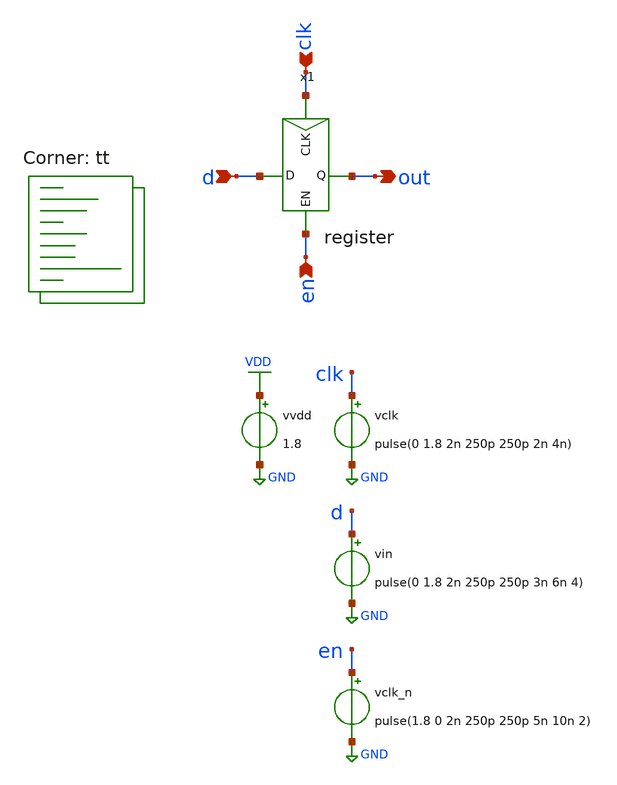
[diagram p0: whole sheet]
** sch_path: xschem/sim/tb_register.sch
**.subckt tb_register out en clk d
*.opin out
*.ipin en
*.ipin clk
*.ipin d
vvdd VDD GND 1.8
vclk clk GND pulse(0 1.8 2n 250p 250p 2n 4n)
vin d GND pulse(0 1.8 2n 250p 250p 3n 6n 4)
vclk_n en GND pulse(1.8 0 2n 250p 250p 5n 10n 2)
x1 clk en out d register
**** begin user architecture code
.lib $::SKYWATER_MODELS/sky130.lib.spice tt


.control
* Transient analysis
TRAN 1p 30n
save all
set filetype=binary
write tb_register_tran.raw
.endc


**** end user architecture code
**.ends

* expanding   symbol:  register.sym # of pins=4
** sym_path: xschem/register.sym
** sch_path: xschem/register.sch
.subckt register CLK EN Q D
*.ipin CLK
*.ipin EN
*.ipin D
*.opin Q
x1 net1 Q D d_flip_flop
x2 CLK EN net2 nand2
x3 net1 net2 inv
.ends


* expanding   symbol:  d_flip_flop.sym # of pins=3
** sym_path: xschem/d_flip_flop.sym
** sch_path: xschem/d_flip_flop.sch
.subckt d_flip_flop clk Q D
*.ipin clk
*.ipin D
*.opin Q
XM1 clk_b clk GND GND sky130_fd_pr__nfet_01v8 L=0.15 W=0.84 nf=1 ad='int((nf+1)/2) * W/nf * 0.29' as='int((nf+2)/2) * W/nf * 0.29'
+ pd='2*int((nf+1)/2) * (W/nf + 0.29)' ps='2*int((nf+2)/2) * (W/nf + 0.29)' nrd='0.29 / W' nrs='0.29 / W'
+ sa=0 sb=0 sd=0 mult=1 m=1
XM2 clk_b clk VDD VDD sky130_fd_pr__pfet_01v8 L=0.15 W=1.68 nf=1 ad='int((nf+1)/2) * W/nf * 0.29' as='int((nf+2)/2) * W/nf * 0.29'
+ pd='2*int((nf+1)/2) * (W/nf + 0.29)' ps='2*int((nf+2)/2) * (W/nf + 0.29)' nrd='0.29 / W' nrs='0.29 / W'
+ sa=0 sb=0 sd=0 mult=1 m=1
XM3 net1 clk net6 VDD sky130_fd_pr__pfet_01v8 L=0.15 W=0.42 nf=1 ad='int((nf+1)/2) * W/nf * 0.29' as='int((nf+2)/2) * W/nf * 0.29'
+ pd='2*int((nf+1)/2) * (W/nf + 0.29)' ps='2*int((nf+2)/2) * (W/nf + 0.29)' nrd='0.29 / W' nrs='0.29 / W'
+ sa=0 sb=0 sd=0 mult=1 m=1
XM4 net6 D VDD VDD sky130_fd_pr__pfet_01v8 L=0.15 W=0.42 nf=1 ad='int((nf+1)/2) * W/nf * 0.29' as='int((nf+2)/2) * W/nf * 0.29'
+ pd='2*int((nf+1)/2) * (W/nf + 0.29)' ps='2*int((nf+2)/2) * (W/nf + 0.29)' nrd='0.29 / W' nrs='0.29 / W'
+ sa=0 sb=0 sd=0 mult=1 m=1
XM5 net1 clk_b net5 GND sky130_fd_pr__nfet_01v8 L=0.15 W=0.42 nf=1 ad='int((nf+1)/2) * W/nf * 0.29' as='int((nf+2)/2) * W/nf * 0.29'
+ pd='2*int((nf+1)/2) * (W/nf + 0.29)' ps='2*int((nf+2)/2) * (W/nf + 0.29)' nrd='0.29 / W' nrs='0.29 / W'
+ sa=0 sb=0 sd=0 mult=1 m=1
XM6 net5 D GND GND sky130_fd_pr__nfet_01v8 L=0.15 W=0.42 nf=1 ad='int((nf+1)/2) * W/nf * 0.29' as='int((nf+2)/2) * W/nf * 0.29'
+ pd='2*int((nf+1)/2) * (W/nf + 0.29)' ps='2*int((nf+2)/2) * (W/nf + 0.29)' nrd='0.29 / W' nrs='0.29 / W'
+ sa=0 sb=0 sd=0 mult=1 m=1
XM7 net2 net1 VDD VDD sky130_fd_pr__pfet_01v8 L=0.15 W=0.42 nf=1 ad='int((nf+1)/2) * W/nf * 0.29' as='int((nf+2)/2) * W/nf * 0.29'
+ pd='2*int((nf+1)/2) * (W/nf + 0.29)' ps='2*int((nf+2)/2) * (W/nf + 0.29)' nrd='0.29 / W' nrs='0.29 / W'
+ sa=0 sb=0 sd=0 mult=1 m=1
XM8 net2 net1 GND GND sky130_fd_pr__nfet_01v8 L=0.15 W=0.42 nf=1 ad='int((nf+1)/2) * W/nf * 0.29' as='int((nf+2)/2) * W/nf * 0.29'
+ pd='2*int((nf+1)/2) * (W/nf + 0.29)' ps='2*int((nf+2)/2) * (W/nf + 0.29)' nrd='0.29 / W' nrs='0.29 / W'
+ sa=0 sb=0 sd=0 mult=1 m=1
XM9 net1 clk_b net4 VDD sky130_fd_pr__pfet_01v8 L=0.15 W=0.42 nf=1 ad='int((nf+1)/2) * W/nf * 0.29' as='int((nf+2)/2) * W/nf * 0.29'
+ pd='2*int((nf+1)/2) * (W/nf + 0.29)' ps='2*int((nf+2)/2) * (W/nf + 0.29)' nrd='0.29 / W' nrs='0.29 / W'
+ sa=0 sb=0 sd=0 mult=1 m=1
XM10 net4 net2 VDD VDD sky130_fd_pr__pfet_01v8 L=0.15 W=0.42 nf=1 ad='int((nf+1)/2) * W/nf * 0.29' as='int((nf+2)/2) * W/nf * 0.29'
+ pd='2*int((nf+1)/2) * (W/nf + 0.29)' ps='2*int((nf+2)/2) * (W/nf + 0.29)' nrd='0.29 / W' nrs='0.29 / W'
+ sa=0 sb=0 sd=0 mult=1 m=1
XM11 net1 clk net3 GND sky130_fd_pr__nfet_01v8 L=0.15 W=0.42 nf=1 ad='int((nf+1)/2) * W/nf * 0.29' as='int((nf+2)/2) * W/nf * 0.29'
+ pd='2*int((nf+1)/2) * (W/nf + 0.29)' ps='2*int((nf+2)/2) * (W/nf + 0.29)' nrd='0.29 / W' nrs='0.29 / W'
+ sa=0 sb=0 sd=0 mult=1 m=1
XM12 net3 net2 GND GND sky130_fd_pr__nfet_01v8 L=0.15 W=0.42 nf=1 ad='int((nf+1)/2) * W/nf * 0.29' as='int((nf+2)/2) * W/nf * 0.29'
+ pd='2*int((nf+1)/2) * (W/nf + 0.29)' ps='2*int((nf+2)/2) * (W/nf + 0.29)' nrd='0.29 / W' nrs='0.29 / W'
+ sa=0 sb=0 sd=0 mult=1 m=1
XM13 net7 clk_b net9 VDD sky130_fd_pr__pfet_01v8 L=0.15 W=0.42 nf=1 ad='int((nf+1)/2) * W/nf * 0.29'
+ as='int((nf+2)/2) * W/nf * 0.29' pd='2*int((nf+1)/2) * (W/nf + 0.29)' ps='2*int((nf+2)/2) * (W/nf + 0.29)'
+ nrd='0.29 / W' nrs='0.29 / W' sa=0 sb=0 sd=0 mult=1 m=1
XM14 net9 net2 VDD VDD sky130_fd_pr__pfet_01v8 L=0.15 W=0.42 nf=1 ad='int((nf+1)/2) * W/nf * 0.29' as='int((nf+2)/2) * W/nf * 0.29'
+ pd='2*int((nf+1)/2) * (W/nf + 0.29)' ps='2*int((nf+2)/2) * (W/nf + 0.29)' nrd='0.29 / W' nrs='0.29 / W'
+ sa=0 sb=0 sd=0 mult=1 m=1
XM15 net7 clk net8 GND sky130_fd_pr__nfet_01v8 L=0.15 W=0.42 nf=1 ad='int((nf+1)/2) * W/nf * 0.29' as='int((nf+2)/2) * W/nf * 0.29'
+ pd='2*int((nf+1)/2) * (W/nf + 0.29)' ps='2*int((nf+2)/2) * (W/nf + 0.29)' nrd='0.29 / W' nrs='0.29 / W'
+ sa=0 sb=0 sd=0 mult=1 m=1
XM16 net8 net2 GND GND sky130_fd_pr__nfet_01v8 L=0.15 W=0.42 nf=1 ad='int((nf+1)/2) * W/nf * 0.29' as='int((nf+2)/2) * W/nf * 0.29'
+ pd='2*int((nf+1)/2) * (W/nf + 0.29)' ps='2*int((nf+2)/2) * (W/nf + 0.29)' nrd='0.29 / W' nrs='0.29 / W'
+ sa=0 sb=0 sd=0 mult=1 m=1
XM17 Q net7 VDD VDD sky130_fd_pr__pfet_01v8 L=0.15 W=0.84 nf=1 ad='int((nf+1)/2) * W/nf * 0.29' as='int((nf+2)/2) * W/nf * 0.29'
+ pd='2*int((nf+1)/2) * (W/nf + 0.29)' ps='2*int((nf+2)/2) * (W/nf + 0.29)' nrd='0.29 / W' nrs='0.29 / W'
+ sa=0 sb=0 sd=0 mult=1 m=1
XM18 Q net7 GND GND sky130_fd_pr__nfet_01v8 L=0.15 W=0.42 nf=1 ad='int((nf+1)/2) * W/nf * 0.29' as='int((nf+2)/2) * W/nf * 0.29'
+ pd='2*int((nf+1)/2) * (W/nf + 0.29)' ps='2*int((nf+2)/2) * (W/nf + 0.29)' nrd='0.29 / W' nrs='0.29 / W'
+ sa=0 sb=0 sd=0 mult=1 m=1
XM19 net7 clk net11 VDD sky130_fd_pr__pfet_01v8 L=0.15 W=0.42 nf=1 ad='int((nf+1)/2) * W/nf * 0.29' as='int((nf+2)/2) * W/nf * 0.29'
+ pd='2*int((nf+1)/2) * (W/nf + 0.29)' ps='2*int((nf+2)/2) * (W/nf + 0.29)' nrd='0.29 / W' nrs='0.29 / W'
+ sa=0 sb=0 sd=0 mult=1 m=1
XM20 net11 Q VDD VDD sky130_fd_pr__pfet_01v8 L=0.15 W=0.42 nf=1 ad='int((nf+1)/2) * W/nf * 0.29' as='int((nf+2)/2) * W/nf * 0.29'
+ pd='2*int((nf+1)/2) * (W/nf + 0.29)' ps='2*int((nf+2)/2) * (W/nf + 0.29)' nrd='0.29 / W' nrs='0.29 / W'
+ sa=0 sb=0 sd=0 mult=1 m=1
XM21 net7 clk_b net10 GND sky130_fd_pr__nfet_01v8 L=0.15 W=0.42 nf=1 ad='int((nf+1)/2) * W/nf * 0.29'
+ as='int((nf+2)/2) * W/nf * 0.29' pd='2*int((nf+1)/2) * (W/nf + 0.29)' ps='2*int((nf+2)/2) * (W/nf + 0.29)'
+ nrd='0.29 / W' nrs='0.29 / W' sa=0 sb=0 sd=0 mult=1 m=1
XM22 net10 Q GND GND sky130_fd_pr__nfet_01v8 L=0.15 W=0.42 nf=1 ad='int((nf+1)/2) * W/nf * 0.29' as='int((nf+2)/2) * W/nf * 0.29'
+ pd='2*int((nf+1)/2) * (W/nf + 0.29)' ps='2*int((nf+2)/2) * (W/nf + 0.29)' nrd='0.29 / W' nrs='0.29 / W'
+ sa=0 sb=0 sd=0 mult=1 m=1
.ends


* expanding   symbol:  nand2.sym # of pins=3
** sym_path: xschem/nand2.sym
** sch_path: xschem/nand2.sch
.subckt nand2 A B Z
*.ipin A
*.ipin B
*.opin Z
XM1 Z A net1 GND sky130_fd_pr__nfet_01v8 L=0.15 W=0.84 nf=1 ad='int((nf+1)/2) * W/nf * 0.29' as='int((nf+2)/2) * W/nf * 0.29'
+ pd='2*int((nf+1)/2) * (W/nf + 0.29)' ps='2*int((nf+2)/2) * (W/nf + 0.29)' nrd='0.29 / W' nrs='0.29 / W'
+ sa=0 sb=0 sd=0 mult=1 m=1
XM2 net1 B GND GND sky130_fd_pr__nfet_01v8 L=0.15 W=0.84 nf=1 ad='int((nf+1)/2) * W/nf * 0.29' as='int((nf+2)/2) * W/nf * 0.29'
+ pd='2*int((nf+1)/2) * (W/nf + 0.29)' ps='2*int((nf+2)/2) * (W/nf + 0.29)' nrd='0.29 / W' nrs='0.29 / W'
+ sa=0 sb=0 sd=0 mult=1 m=1
XM3 Z B VDD VDD sky130_fd_pr__pfet_01v8 L=0.15 W=0.84 nf=1 ad='int((nf+1)/2) * W/nf * 0.29' as='int((nf+2)/2) * W/nf * 0.29'
+ pd='2*int((nf+1)/2) * (W/nf + 0.29)' ps='2*int((nf+2)/2) * (W/nf + 0.29)' nrd='0.29 / W' nrs='0.29 / W'
+ sa=0 sb=0 sd=0 mult=1 m=1
XM4 Z A VDD VDD sky130_fd_pr__pfet_01v8 L=0.15 W=0.84 nf=1 ad='int((nf+1)/2) * W/nf * 0.29' as='int((nf+2)/2) * W/nf * 0.29'
+ pd='2*int((nf+1)/2) * (W/nf + 0.29)' ps='2*int((nf+2)/2) * (W/nf + 0.29)' nrd='0.29 / W' nrs='0.29 / W'
+ sa=0 sb=0 sd=0 mult=1 m=1
.ends


* expanding   symbol:  inv.sym # of pins=2
** sym_path: xschem/inv.sym
** sch_path: xschem/inv.sch
.subckt inv Z A
*.ipin a
*.opin z
XM1 z a GND GND sky130_fd_pr__nfet_01v8 L=0.15 W=0.42 nf=1 ad='int((nf+1)/2) * W/nf * 0.29' as='int((nf+2)/2) * W/nf * 0.29'
+ pd='2*int((nf+1)/2) * (W/nf + 0.29)' ps='2*int((nf+2)/2) * (W/nf + 0.29)' nrd='0.29 / W' nrs='0.29 / W'
+ sa=0 sb=0 sd=0 mult=1 m=1
XM2 z a VDD VDD sky130_fd_pr__pfet_01v8 L=0.15 W=0.84 nf=1 ad='int((nf+1)/2) * W/nf * 0.29' as='int((nf+2)/2) * W/nf * 0.29'
+ pd='2*int((nf+1)/2) * (W/nf + 0.29)' ps='2*int((nf+2)/2) * (W/nf + 0.29)' nrd='0.29 / W' nrs='0.29 / W'
+ sa=0 sb=0 sd=0 mult=1 m=1
.ends

.GLOBAL VDD
.GLOBAL GND
.end
